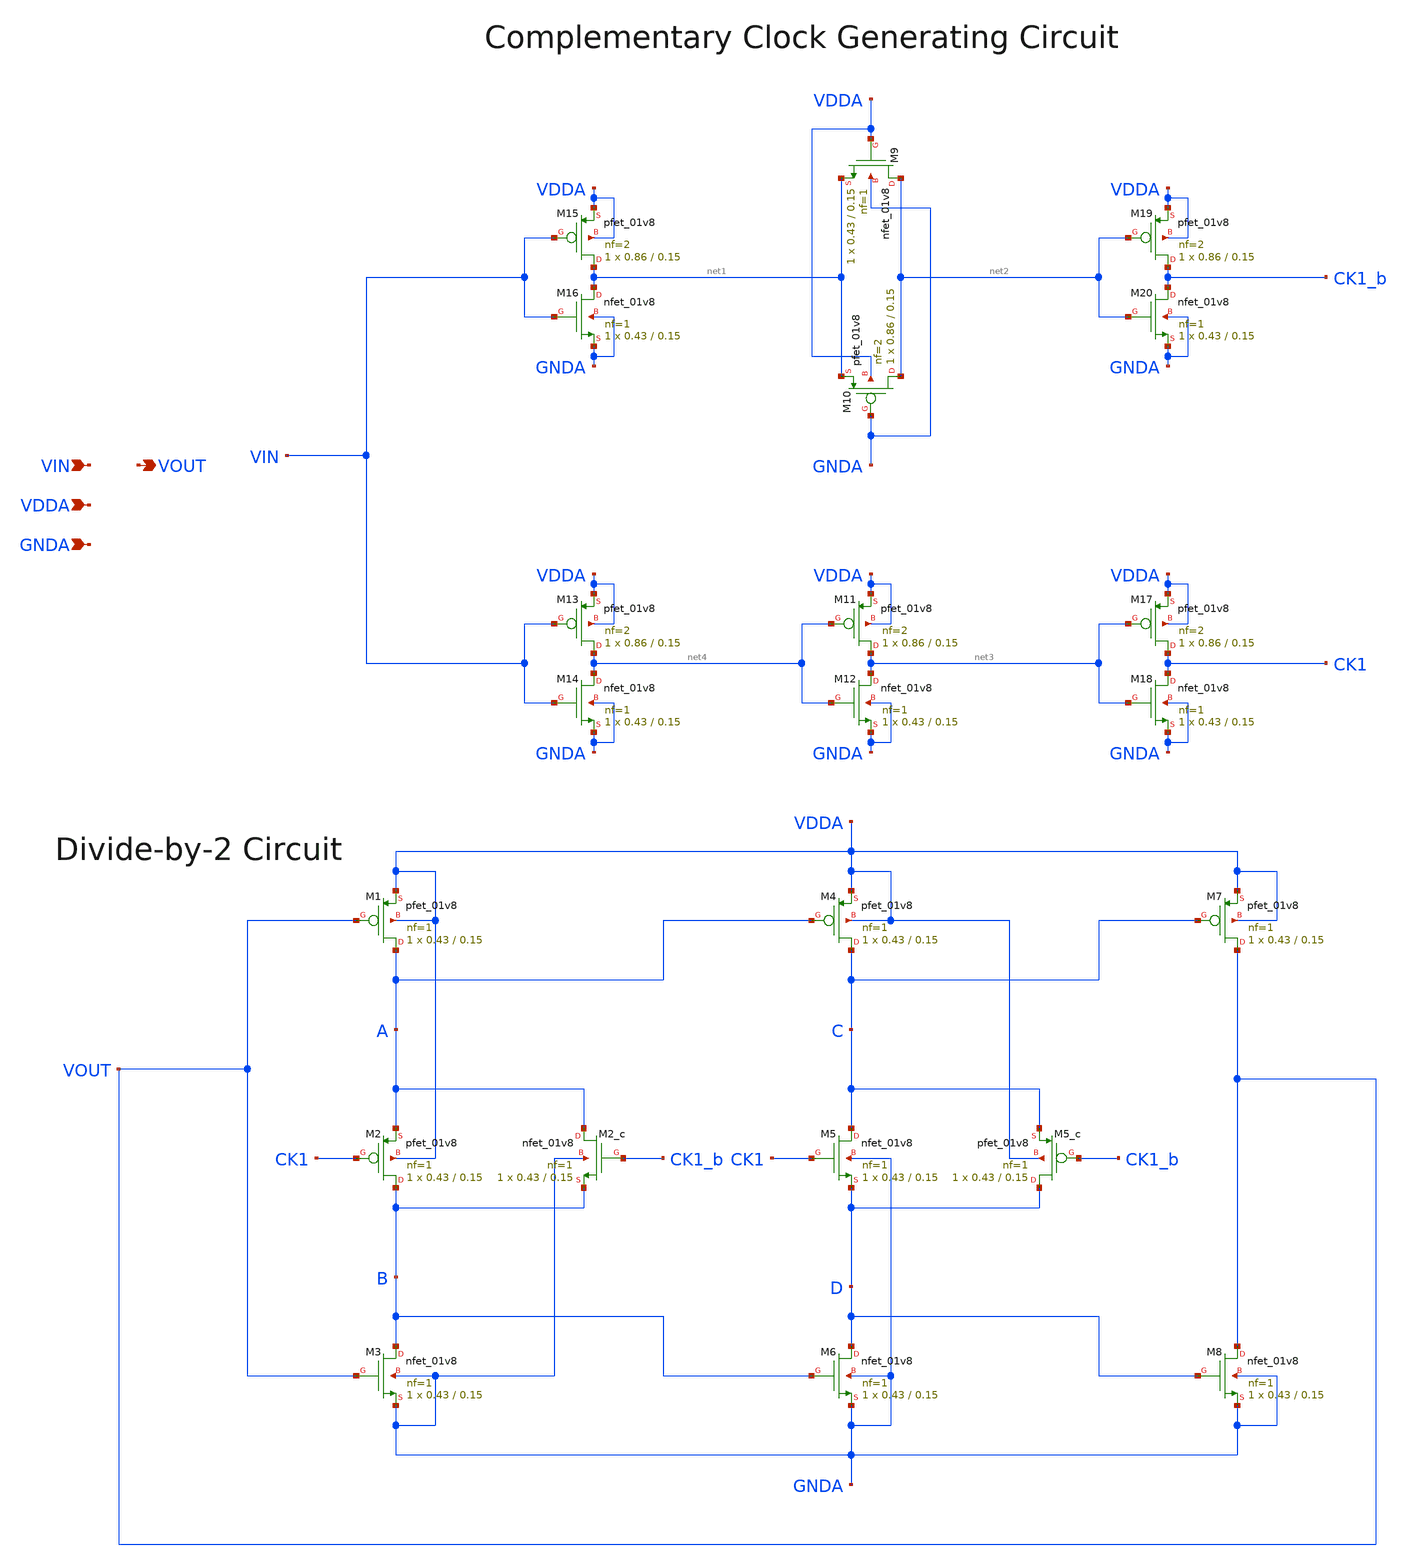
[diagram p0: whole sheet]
** sch_path: projects/pll/divider/xschem_ngspice/FF_comp_sw_divide2_2.sch
**.subckt FF_comp_sw_divide2_2 VIN VOUT VDDA GNDA
*.ipin VIN
*.opin VOUT
*.ipin VDDA
*.ipin GNDA
XM7 VOUT C VDDA VDDA sky130_fd_pr__pfet_01v8 L=0.15 W=0.43 nf=1 ad='int((nf+1)/2) * W/nf * 0.29' as='int((nf+2)/2) * W/nf * 0.29'
+ pd='2*int((nf+1)/2) * (W/nf + 0.29)' ps='2*int((nf+2)/2) * (W/nf + 0.29)' nrd='0.29 / W' nrs='0.29 / W'
+ sa=0 sb=0 sd=0 mult=1 m=1
XM5 C CK1 D GNDA sky130_fd_pr__nfet_01v8 L=0.15 W=0.43 nf=1 ad='int((nf+1)/2) * W/nf * 0.29' as='int((nf+2)/2) * W/nf * 0.29'
+ pd='2*int((nf+1)/2) * (W/nf + 0.29)' ps='2*int((nf+2)/2) * (W/nf + 0.29)' nrd='0.29 / W' nrs='0.29 / W'
+ sa=0 sb=0 sd=0 mult=1 m=1
XM8 VOUT D GNDA GNDA sky130_fd_pr__nfet_01v8 L=0.15 W=0.43 nf=1 ad='int((nf+1)/2) * W/nf * 0.29' as='int((nf+2)/2) * W/nf * 0.29'
+ pd='2*int((nf+1)/2) * (W/nf + 0.29)' ps='2*int((nf+2)/2) * (W/nf + 0.29)' nrd='0.29 / W' nrs='0.29 / W'
+ sa=0 sb=0 sd=0 mult=1 m=1
XM4 C A VDDA VDDA sky130_fd_pr__pfet_01v8 L=0.15 W=0.43 nf=1 ad='int((nf+1)/2) * W/nf * 0.29' as='int((nf+2)/2) * W/nf * 0.29'
+ pd='2*int((nf+1)/2) * (W/nf + 0.29)' ps='2*int((nf+2)/2) * (W/nf + 0.29)' nrd='0.29 / W' nrs='0.29 / W'
+ sa=0 sb=0 sd=0 mult=1 m=1
XM6 D B GNDA GNDA sky130_fd_pr__nfet_01v8 L=0.15 W=0.43 nf=1 ad='int((nf+1)/2) * W/nf * 0.29' as='int((nf+2)/2) * W/nf * 0.29'
+ pd='2*int((nf+1)/2) * (W/nf + 0.29)' ps='2*int((nf+2)/2) * (W/nf + 0.29)' nrd='0.29 / W' nrs='0.29 / W'
+ sa=0 sb=0 sd=0 mult=1 m=1
XM1 A VOUT VDDA VDDA sky130_fd_pr__pfet_01v8 L=0.15 W=0.43 nf=1 ad='int((nf+1)/2) * W/nf * 0.29' as='int((nf+2)/2) * W/nf * 0.29'
+ pd='2*int((nf+1)/2) * (W/nf + 0.29)' ps='2*int((nf+2)/2) * (W/nf + 0.29)' nrd='0.29 / W' nrs='0.29 / W'
+ sa=0 sb=0 sd=0 mult=1 m=1
XM3 B VOUT GNDA GNDA sky130_fd_pr__nfet_01v8 L=0.15 W=0.43 nf=1 ad='int((nf+1)/2) * W/nf * 0.29' as='int((nf+2)/2) * W/nf * 0.29'
+ pd='2*int((nf+1)/2) * (W/nf + 0.29)' ps='2*int((nf+2)/2) * (W/nf + 0.29)' nrd='0.29 / W' nrs='0.29 / W'
+ sa=0 sb=0 sd=0 mult=1 m=1
XM2 B CK1 A VDDA sky130_fd_pr__pfet_01v8 L=0.15 W=0.43 nf=1 ad='int((nf+1)/2) * W/nf * 0.29' as='int((nf+2)/2) * W/nf * 0.29'
+ pd='2*int((nf+1)/2) * (W/nf + 0.29)' ps='2*int((nf+2)/2) * (W/nf + 0.29)' nrd='0.29 / W' nrs='0.29 / W'
+ sa=0 sb=0 sd=0 mult=1 m=1
XM5_c D CK1_b C VDDA sky130_fd_pr__pfet_01v8 L=0.15 W=0.43 nf=1 ad='int((nf+1)/2) * W/nf * 0.29' as='int((nf+2)/2) * W/nf * 0.29'
+ pd='2*int((nf+1)/2) * (W/nf + 0.29)' ps='2*int((nf+2)/2) * (W/nf + 0.29)' nrd='0.29 / W' nrs='0.29 / W'
+ sa=0 sb=0 sd=0 mult=1 m=1
XM2_c A CK1_b B GNDA sky130_fd_pr__nfet_01v8 L=0.15 W=0.43 nf=1 ad='int((nf+1)/2) * W/nf * 0.29' as='int((nf+2)/2) * W/nf * 0.29'
+ pd='2*int((nf+1)/2) * (W/nf + 0.29)' ps='2*int((nf+2)/2) * (W/nf + 0.29)' nrd='0.29 / W' nrs='0.29 / W'
+ sa=0 sb=0 sd=0 mult=1 m=1
XM10 net2 GNDA net1 VDDA sky130_fd_pr__pfet_01v8 L=0.15 W=0.86 nf=2 ad='int((nf+1)/2) * W/nf * 0.29'
+ as='int((nf+2)/2) * W/nf * 0.29' pd='2*int((nf+1)/2) * (W/nf + 0.29)' ps='2*int((nf+2)/2) * (W/nf + 0.29)'
+ nrd='0.29 / W' nrs='0.29 / W' sa=0 sb=0 sd=0 mult=1 m=1
XM9 net2 VDDA net1 GNDA sky130_fd_pr__nfet_01v8 L=0.15 W=0.43 nf=1 ad='int((nf+1)/2) * W/nf * 0.29' as='int((nf+2)/2) * W/nf * 0.29'
+ pd='2*int((nf+1)/2) * (W/nf + 0.29)' ps='2*int((nf+2)/2) * (W/nf + 0.29)' nrd='0.29 / W' nrs='0.29 / W'
+ sa=0 sb=0 sd=0 mult=1 m=1
XM11 net3 net4 VDDA VDDA sky130_fd_pr__pfet_01v8 L=0.15 W=0.86 nf=2 ad='int((nf+1)/2) * W/nf * 0.29'
+ as='int((nf+2)/2) * W/nf * 0.29' pd='2*int((nf+1)/2) * (W/nf + 0.29)' ps='2*int((nf+2)/2) * (W/nf + 0.29)'
+ nrd='0.29 / W' nrs='0.29 / W' sa=0 sb=0 sd=0 mult=1 m=1
XM12 net3 net4 GNDA GNDA sky130_fd_pr__nfet_01v8 L=0.15 W=0.43 nf=1 ad='int((nf+1)/2) * W/nf * 0.29'
+ as='int((nf+2)/2) * W/nf * 0.29' pd='2*int((nf+1)/2) * (W/nf + 0.29)' ps='2*int((nf+2)/2) * (W/nf + 0.29)'
+ nrd='0.29 / W' nrs='0.29 / W' sa=0 sb=0 sd=0 mult=1 m=1
XM13 net4 VIN VDDA VDDA sky130_fd_pr__pfet_01v8 L=0.15 W=0.86 nf=2 ad='int((nf+1)/2) * W/nf * 0.29' as='int((nf+2)/2) * W/nf * 0.29'
+ pd='2*int((nf+1)/2) * (W/nf + 0.29)' ps='2*int((nf+2)/2) * (W/nf + 0.29)' nrd='0.29 / W' nrs='0.29 / W'
+ sa=0 sb=0 sd=0 mult=1 m=1
XM14 net4 VIN GNDA GNDA sky130_fd_pr__nfet_01v8 L=0.15 W=0.43 nf=1 ad='int((nf+1)/2) * W/nf * 0.29' as='int((nf+2)/2) * W/nf * 0.29'
+ pd='2*int((nf+1)/2) * (W/nf + 0.29)' ps='2*int((nf+2)/2) * (W/nf + 0.29)' nrd='0.29 / W' nrs='0.29 / W'
+ sa=0 sb=0 sd=0 mult=1 m=1
XM15 net1 VIN VDDA VDDA sky130_fd_pr__pfet_01v8 L=0.15 W=0.86 nf=2 ad='int((nf+1)/2) * W/nf * 0.29' as='int((nf+2)/2) * W/nf * 0.29'
+ pd='2*int((nf+1)/2) * (W/nf + 0.29)' ps='2*int((nf+2)/2) * (W/nf + 0.29)' nrd='0.29 / W' nrs='0.29 / W'
+ sa=0 sb=0 sd=0 mult=1 m=1
XM16 net1 VIN GNDA GNDA sky130_fd_pr__nfet_01v8 L=0.15 W=0.43 nf=1 ad='int((nf+1)/2) * W/nf * 0.29' as='int((nf+2)/2) * W/nf * 0.29'
+ pd='2*int((nf+1)/2) * (W/nf + 0.29)' ps='2*int((nf+2)/2) * (W/nf + 0.29)' nrd='0.29 / W' nrs='0.29 / W'
+ sa=0 sb=0 sd=0 mult=1 m=1
XM17 CK1 net3 VDDA VDDA sky130_fd_pr__pfet_01v8 L=0.15 W=0.86 nf=2 ad='int((nf+1)/2) * W/nf * 0.29' as='int((nf+2)/2) * W/nf * 0.29'
+ pd='2*int((nf+1)/2) * (W/nf + 0.29)' ps='2*int((nf+2)/2) * (W/nf + 0.29)' nrd='0.29 / W' nrs='0.29 / W'
+ sa=0 sb=0 sd=0 mult=1 m=1
XM18 CK1 net3 GNDA GNDA sky130_fd_pr__nfet_01v8 L=0.15 W=0.43 nf=1 ad='int((nf+1)/2) * W/nf * 0.29' as='int((nf+2)/2) * W/nf * 0.29'
+ pd='2*int((nf+1)/2) * (W/nf + 0.29)' ps='2*int((nf+2)/2) * (W/nf + 0.29)' nrd='0.29 / W' nrs='0.29 / W'
+ sa=0 sb=0 sd=0 mult=1 m=1
XM19 CK1_b net2 VDDA VDDA sky130_fd_pr__pfet_01v8 L=0.15 W=0.86 nf=2 ad='int((nf+1)/2) * W/nf * 0.29'
+ as='int((nf+2)/2) * W/nf * 0.29' pd='2*int((nf+1)/2) * (W/nf + 0.29)' ps='2*int((nf+2)/2) * (W/nf + 0.29)'
+ nrd='0.29 / W' nrs='0.29 / W' sa=0 sb=0 sd=0 mult=1 m=1
XM20 CK1_b net2 GNDA GNDA sky130_fd_pr__nfet_01v8 L=0.15 W=0.43 nf=1 ad='int((nf+1)/2) * W/nf * 0.29'
+ as='int((nf+2)/2) * W/nf * 0.29' pd='2*int((nf+1)/2) * (W/nf + 0.29)' ps='2*int((nf+2)/2) * (W/nf + 0.29)'
+ nrd='0.29 / W' nrs='0.29 / W' sa=0 sb=0 sd=0 mult=1 m=1
**.ends
.end
